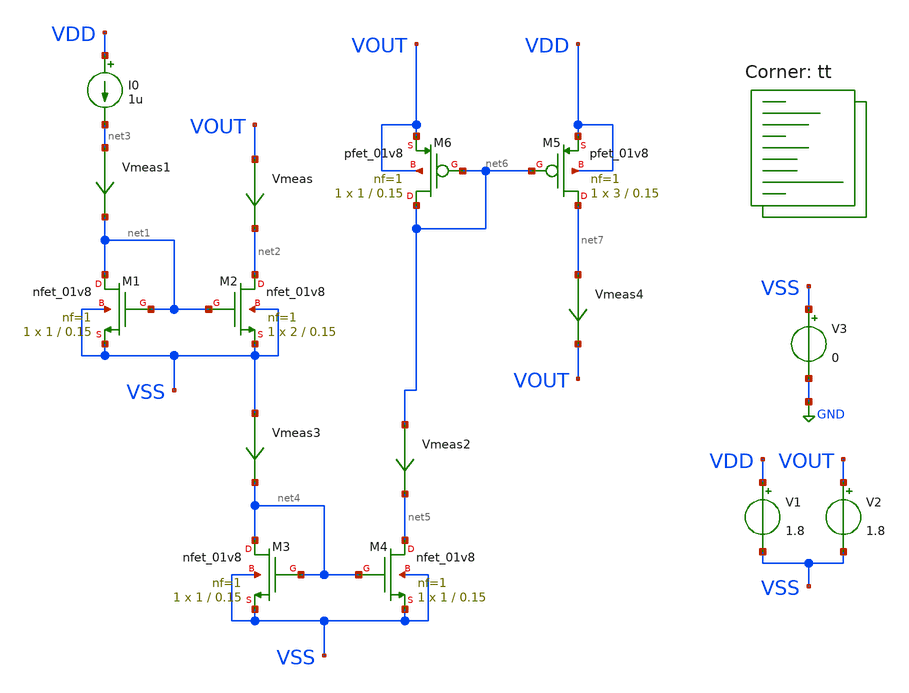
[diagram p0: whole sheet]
** sch_path: week02_current_diffpair/tugas4_basic_current_mirror/cmos-current-mirror.sch
**.subckt cmos-current-mirror
XM1 net1 net1 VSS VSS sky130_fd_pr__nfet_01v8 L=0.15 W=1 nf=1 ad='int((nf+1)/2) * W/nf * 0.29' as='int((nf+2)/2) * W/nf * 0.29'
+ pd='2*int((nf+1)/2) * (W/nf + 0.29)' ps='2*int((nf+2)/2) * (W/nf + 0.29)' nrd='0.29 / W' nrs='0.29 / W'
+ sa=0 sb=0 sd=0 mult=1 m=1
XM2 net2 net1 VSS VSS sky130_fd_pr__nfet_01v8 L=0.15 W=2 nf=1 ad='int((nf+1)/2) * W/nf * 0.29' as='int((nf+2)/2) * W/nf * 0.29'
+ pd='2*int((nf+1)/2) * (W/nf + 0.29)' ps='2*int((nf+2)/2) * (W/nf + 0.29)' nrd='0.29 / W' nrs='0.29 / W'
+ sa=0 sb=0 sd=0 mult=1 m=1
I0 VDD net3 1u
Vmeas VOUT net2 0
.save i(vmeas)
Vmeas1 net3 net1 0
.save i(vmeas1)
XM3 net4 net4 VSS VSS sky130_fd_pr__nfet_01v8 L=0.15 W=1 nf=1 ad='int((nf+1)/2) * W/nf * 0.29' as='int((nf+2)/2) * W/nf * 0.29'
+ pd='2*int((nf+1)/2) * (W/nf + 0.29)' ps='2*int((nf+2)/2) * (W/nf + 0.29)' nrd='0.29 / W' nrs='0.29 / W'
+ sa=0 sb=0 sd=0 mult=1 m=1
XM4 net5 net4 VSS VSS sky130_fd_pr__nfet_01v8 L=0.15 W=1 nf=1 ad='int((nf+1)/2) * W/nf * 0.29' as='int((nf+2)/2) * W/nf * 0.29'
+ pd='2*int((nf+1)/2) * (W/nf + 0.29)' ps='2*int((nf+2)/2) * (W/nf + 0.29)' nrd='0.29 / W' nrs='0.29 / W'
+ sa=0 sb=0 sd=0 mult=1 m=1
Vmeas2 net6 net5 0
.save i(vmeas2)
Vmeas3 VSS net4 0
.save i(vmeas3)
XM5 net7 net6 VDD VDD sky130_fd_pr__pfet_01v8 L=0.15 W=3 nf=1 ad='int((nf+1)/2) * W/nf * 0.29' as='int((nf+2)/2) * W/nf * 0.29'
+ pd='2*int((nf+1)/2) * (W/nf + 0.29)' ps='2*int((nf+2)/2) * (W/nf + 0.29)' nrd='0.29 / W' nrs='0.29 / W'
+ sa=0 sb=0 sd=0 mult=1 m=1
XM6 net6 net6 VOUT VOUT sky130_fd_pr__pfet_01v8 L=0.15 W=1 nf=1 ad='int((nf+1)/2) * W/nf * 0.29' as='int((nf+2)/2) * W/nf * 0.29'
+ pd='2*int((nf+1)/2) * (W/nf + 0.29)' ps='2*int((nf+2)/2) * (W/nf + 0.29)' nrd='0.29 / W' nrs='0.29 / W'
+ sa=0 sb=0 sd=0 mult=1 m=1
Vmeas4 net7 VOUT 0
.save i(vmeas4)
V1 VDD VSS 1.8
V2 VOUT VSS 1.8
V3 VSS GND 0
**** begin user architecture code
.lib $::SKYWATER_MODELS/sky130.lib.spice tt



	.param Wm2=1u

.control
	dc V2 0 1.8 0.01
	plot I(Vmeas)
	plot I(Vmeas2)
	plot I(Vmeas4)

saveall
.endc


**** end user architecture code
**.ends
.GLOBAL GND
.end
